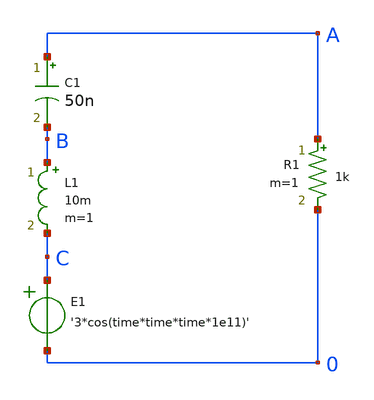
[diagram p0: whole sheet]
** sch_path: sandbox/test1.sch
**.subckt test1
R1 A 0 1k m=1
C1 A B 50n m=1
L1 B C 10m m=1
E1 C 0 VOL=' '3*cos(time*time*time*1e11)' '
**** begin user architecture code


.tran 10n 2000u uic
.save all


**** end user architecture code
**.ends
.end
